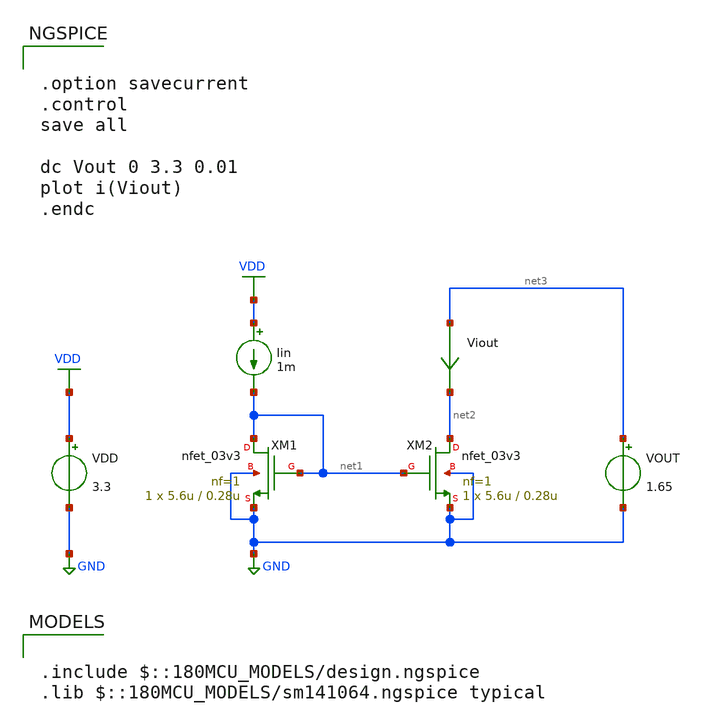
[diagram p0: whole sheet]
** sch_path: fifty_nifty/07_cm_dc2.sch
**.subckt 07_cm_dc2
XM1 net1 net1 GND GND nfet_03v3 L=0.28u W=5.6u nf=1 ad='int((nf+1)/2) * W/nf * 0.18u' as='int((nf+2)/2) * W/nf * 0.18u'
+ pd='2*int((nf+1)/2) * (W/nf + 0.18u)' ps='2*int((nf+2)/2) * (W/nf + 0.18u)' nrd='0.18u / W' nrs='0.18u / W'
+ sa=0 sb=0 sd=0 m=1
VOUT net3 GND 1.65
Viout net3 net2 0
.save i(viout)
VDD VDD GND 3.3
XM2 net2 net1 GND GND nfet_03v3 L=0.28u W=5.6u nf=1 ad='int((nf+1)/2) * W/nf * 0.18u' as='int((nf+2)/2) * W/nf * 0.18u'
+ pd='2*int((nf+1)/2) * (W/nf + 0.18u)' ps='2*int((nf+2)/2) * (W/nf + 0.18u)' nrd='0.18u / W' nrs='0.18u / W'
+ sa=0 sb=0 sd=0 m=1
Iin VDD net1 1m
**** begin user architecture code

.option savecurrent
.control
save all

dc Vout 0 3.3 0.01
plot i(Viout)
.endc


.include $::180MCU_MODELS/design.ngspice
.lib $::180MCU_MODELS/sm141064.ngspice typical

**** end user architecture code
**.ends
.GLOBAL GND
.GLOBAL VDD
.end
